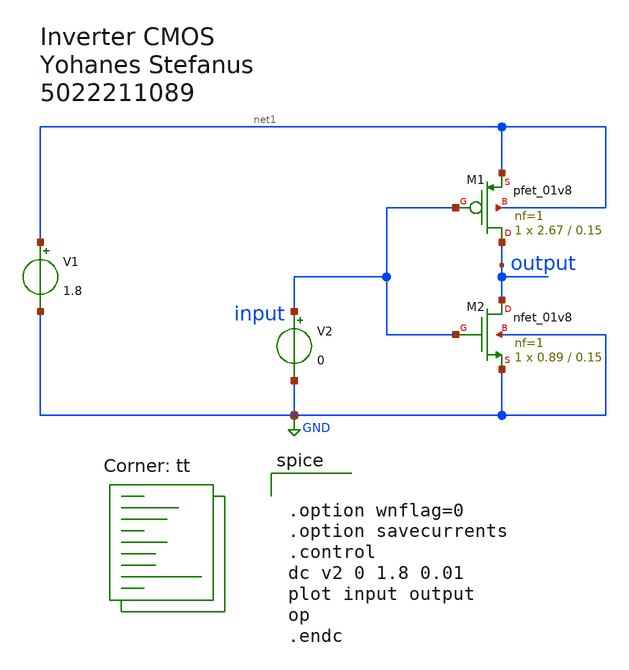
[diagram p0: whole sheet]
** sch_path: tugas_inverter_Yohanes.sch
**.subckt tugas_inverter_Yohanes
XM1 output input net1 net1 sky130_fd_pr__pfet_01v8 L=0.15 W=2.67 nf=1 ad='int((nf+1)/2) * W/nf * 0.29'
+ as='int((nf+2)/2) * W/nf * 0.29' pd='2*int((nf+1)/2) * (W/nf + 0.29)' ps='2*int((nf+2)/2) * (W/nf + 0.29)'
+ nrd='0.29 / W' nrs='0.29 / W' sa=0 sb=0 sd=0 mult=1 m=1
XM2 output input GND GND sky130_fd_pr__nfet_01v8 L=0.15 W=0.89 nf=1 ad='int((nf+1)/2) * W/nf * 0.29'
+ as='int((nf+2)/2) * W/nf * 0.29' pd='2*int((nf+1)/2) * (W/nf + 0.29)' ps='2*int((nf+2)/2) * (W/nf + 0.29)'
+ nrd='0.29 / W' nrs='0.29 / W' sa=0 sb=0 sd=0 mult=1 m=1
V1 net1 GND 1.8
V2 input GND 0
**** begin user architecture code
.lib $::SKYWATER_MODELS/sky130.lib.spice tt


.option wnflag=0
.option savecurrents
.control
dc v2 0 1.8 0.01
plot input output
op
.endc


**** end user architecture code
**.ends
.GLOBAL GND
.end
